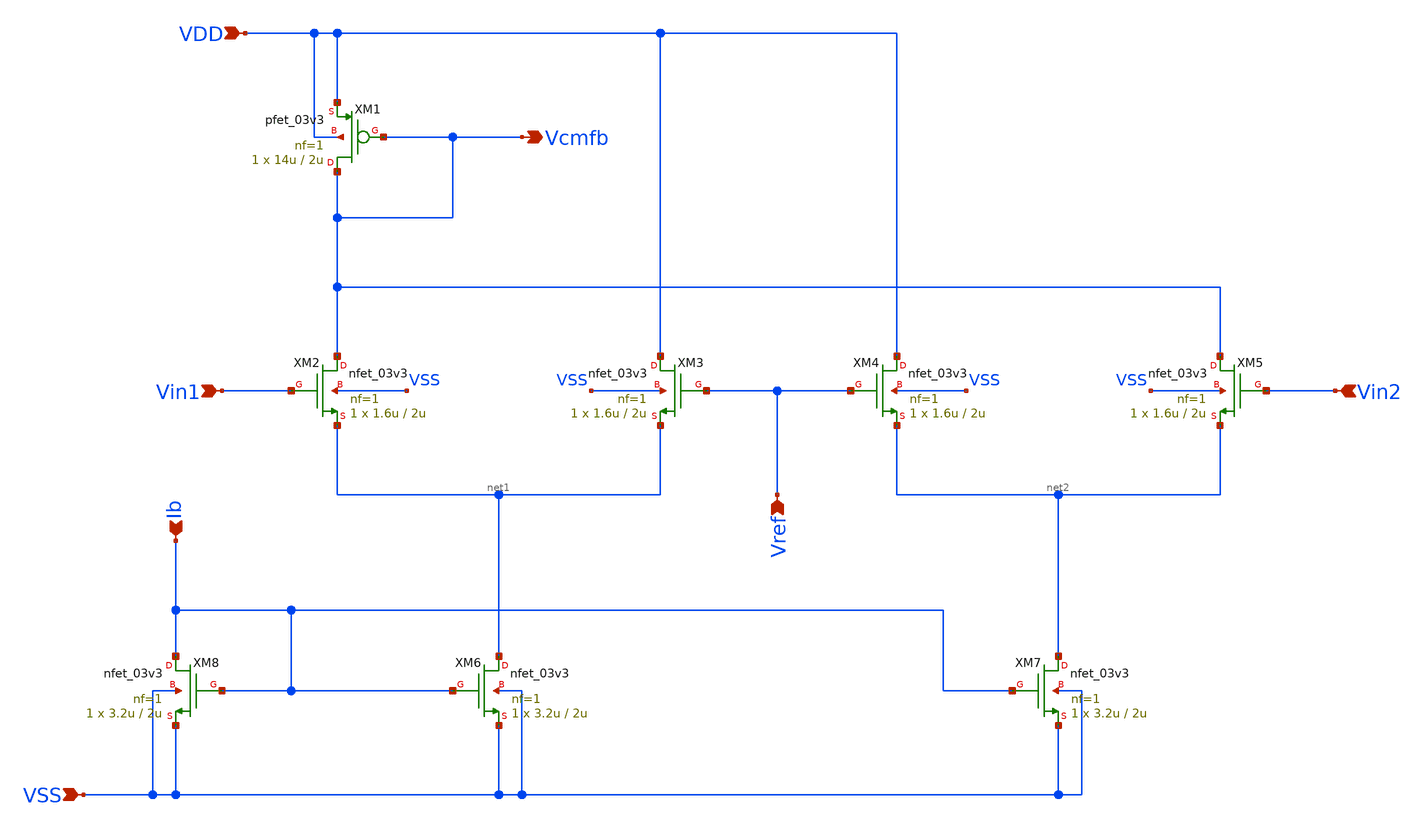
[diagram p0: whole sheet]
** sch_path: designs/libs/core_ina/ina_cmfb/ina_cmfb.sch
**.subckt ina_cmfb Vin1 Vin2 Vcmfb Vref VSS Ib VDD
*.ipin Vin1
*.ipin Vin2
*.opin Vcmfb
*.ipin Vref
*.ipin VSS
*.ipin Ib
*.ipin VDD
XM1 Vcmfb Vcmfb VDD VDD pfet_03v3 L=2u W=14u nf=1 ad='int((nf+1)/2) * W/nf * 0.18u' as='int((nf+2)/2) * W/nf * 0.18u'
+ pd='2*int((nf+1)/2) * (W/nf + 0.18u)' ps='2*int((nf+2)/2) * (W/nf + 0.18u)' nrd='0.18u / W' nrs='0.18u / W'
+ sa=0 sb=0 sd=0 m=1
XM2 Vcmfb Vin1 net1 VSS nfet_03v3 L=2u W=1.6u nf=1 ad='int((nf+1)/2) * W/nf * 0.18u' as='int((nf+2)/2) * W/nf * 0.18u'
+ pd='2*int((nf+1)/2) * (W/nf + 0.18u)' ps='2*int((nf+2)/2) * (W/nf + 0.18u)' nrd='0.18u / W' nrs='0.18u / W'
+ sa=0 sb=0 sd=0 m=1
XM3 VDD Vref net1 VSS nfet_03v3 L=2u W=1.6u nf=1 ad='int((nf+1)/2) * W/nf * 0.18u' as='int((nf+2)/2) * W/nf * 0.18u'
+ pd='2*int((nf+1)/2) * (W/nf + 0.18u)' ps='2*int((nf+2)/2) * (W/nf + 0.18u)' nrd='0.18u / W' nrs='0.18u / W'
+ sa=0 sb=0 sd=0 m=1
XM6 net1 Ib VSS VSS nfet_03v3 L=2u W=3.2u nf=1 ad='int((nf+1)/2) * W/nf * 0.18u' as='int((nf+2)/2) * W/nf * 0.18u'
+ pd='2*int((nf+1)/2) * (W/nf + 0.18u)' ps='2*int((nf+2)/2) * (W/nf + 0.18u)' nrd='0.18u / W' nrs='0.18u / W'
+ sa=0 sb=0 sd=0 m=1
XM4 VDD Vref net2 VSS nfet_03v3 L=2u W=1.6u nf=1 ad='int((nf+1)/2) * W/nf * 0.18u' as='int((nf+2)/2) * W/nf * 0.18u'
+ pd='2*int((nf+1)/2) * (W/nf + 0.18u)' ps='2*int((nf+2)/2) * (W/nf + 0.18u)' nrd='0.18u / W' nrs='0.18u / W'
+ sa=0 sb=0 sd=0 m=1
XM5 Vcmfb Vin2 net2 VSS nfet_03v3 L=2u W=1.6u nf=1 ad='int((nf+1)/2) * W/nf * 0.18u' as='int((nf+2)/2) * W/nf * 0.18u'
+ pd='2*int((nf+1)/2) * (W/nf + 0.18u)' ps='2*int((nf+2)/2) * (W/nf + 0.18u)' nrd='0.18u / W' nrs='0.18u / W'
+ sa=0 sb=0 sd=0 m=1
XM7 net2 Ib VSS VSS nfet_03v3 L=2u W=3.2u nf=1 ad='int((nf+1)/2) * W/nf * 0.18u' as='int((nf+2)/2) * W/nf * 0.18u'
+ pd='2*int((nf+1)/2) * (W/nf + 0.18u)' ps='2*int((nf+2)/2) * (W/nf + 0.18u)' nrd='0.18u / W' nrs='0.18u / W'
+ sa=0 sb=0 sd=0 m=1
XM8 Ib Ib VSS VSS nfet_03v3 L=2u W=3.2u nf=1 ad='int((nf+1)/2) * W/nf * 0.18u' as='int((nf+2)/2) * W/nf * 0.18u'
+ pd='2*int((nf+1)/2) * (W/nf + 0.18u)' ps='2*int((nf+2)/2) * (W/nf + 0.18u)' nrd='0.18u / W' nrs='0.18u / W'
+ sa=0 sb=0 sd=0 m=1
**.ends
.end
